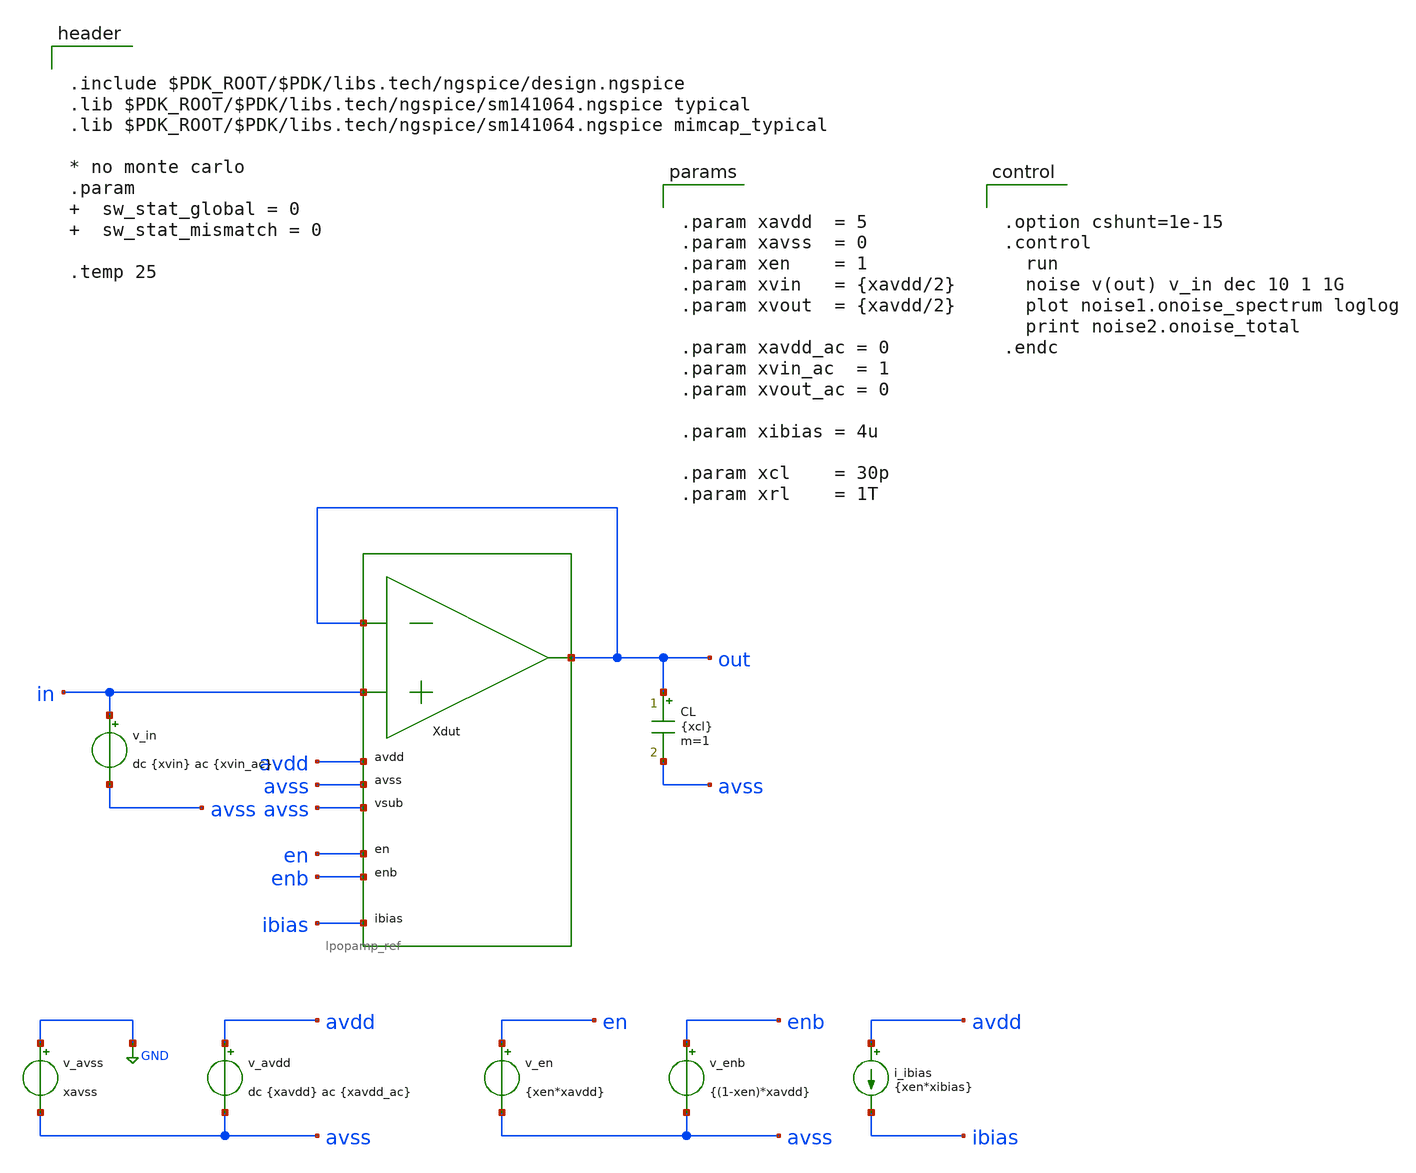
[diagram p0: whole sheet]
** sch_path: xschem/tb_lpopamp_buf_noise.sch
**.subckt tb_lpopamp_buf_noise
Xdut out in out avdd avss avss en enb ibias lpopamp_ref
v_avss GND avss xavss
v_avdd avdd avss dc {xavdd} ac {xavdd_ac}
v_in in avss dc {xvin} ac {xvin_ac}
v_en en avss {xen*xavdd}
v_enb enb avss {(1-xen)*xavdd}
i_ibias avdd ibias {xen*xibias}
CL out avss {xcl} m=1
**** begin user architecture code


.include $PDK_ROOT/$PDK/libs.tech/ngspice/design.ngspice
.lib $PDK_ROOT/$PDK/libs.tech/ngspice/sm141064.ngspice typical
.lib $PDK_ROOT/$PDK/libs.tech/ngspice/sm141064.ngspice mimcap_typical

* no monte carlo
.param   sw_stat_global = 0   sw_stat_mismatch = 0

.temp 25




.option cshunt=1e-15
.control
  run
  noise v(out) v_in dec 10 1 1G
  plot noise1.onoise_spectrum loglog
  print noise2.onoise_total
.endc




.param xavdd  = 5
.param xavss  = 0
.param xen    = 1
.param xvin   = {xavdd/2}
.param xvout  = {xavdd/2}

.param xavdd_ac = 0
.param xvin_ac  = 1
.param xvout_ac = 0

.param xibias = 4u

.param xcl    = 30p
.param xrl    = 1T


**** end user architecture code
**.ends
.GLOBAL GND
.end
